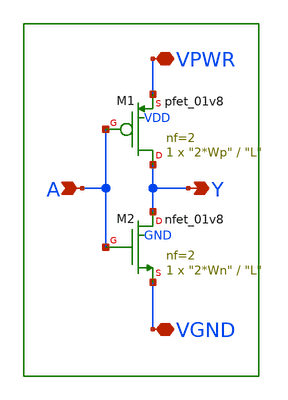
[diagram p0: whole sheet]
** sch_path: xschem/lib/main_inv.sch
**.subckt main_inv VPWR VGND A Y
*.iopin VPWR
*.iopin VGND
*.ipin A
*.opin Y
XM1 Y A VPWR VDD sky130_fd_pr__pfet_01v8 L="L" W="2*Wp" nf=2 ad='int((2 + 1)/2) * "2*Wp" / 2 * 0.29'
+ as='int((2 + 2)/2) * "2*Wp" / 2 * 0.29' pd='2*int((2 + 1)/2) * ("2*Wp" / 2 + 0.29)' ps='2*int((2 + 2)/2) * ("2*Wp" / 2 + 0.29)'
+ nrd='0.29 / "2*Wp" ' nrs='0.29 / "2*Wp" ' sa=0 sb=0 sd=0 mult=1 m=1
XM2 Y A VGND GND sky130_fd_pr__nfet_01v8 L="L" W="2*Wn" nf=2 ad='int((nf+1)/2) * W/nf * 0.29' as='int((nf+2)/2) * W/nf * 0.29'
+ pd='2*int((nf+1)/2) * (W/nf + 0.29)' ps='2*int((nf+2)/2) * (W/nf + 0.29)' nrd='0.29 / W' nrs='0.29 / W'
+ sa=0 sb=0 sd=0 mult=1 m=1
**.ends
.end
